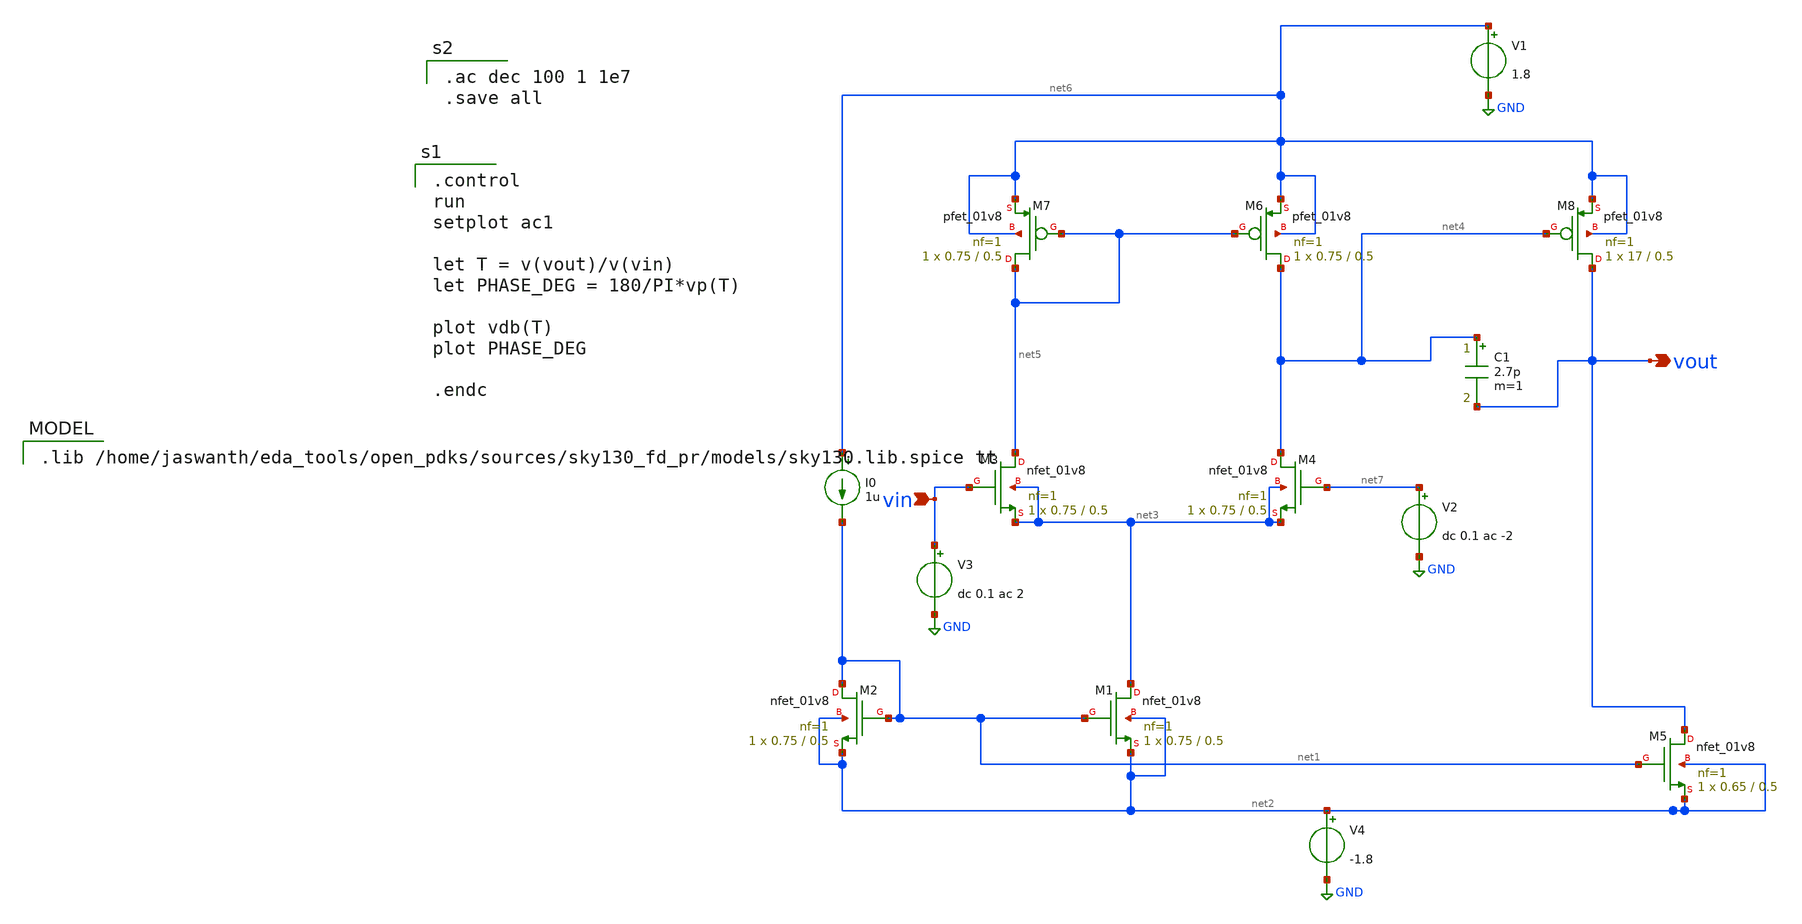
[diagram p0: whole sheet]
** sch_path: TwoStage_OpAmp/TwoStage_Main.sch
**.subckt TwoStage_Main vout vin
*.opin vout
*.ipin vin
XM1 net3 net1 net2 net2 sky130_fd_pr__nfet_01v8 L=0.5 W=0.75 nf=1 ad='int((1 + 1)/2) * 0.75 / 1 * 0.29'
+ as='int((1 + 2)/2) * 0.75 / 1 * 0.29' pd='2*int((1 + 1)/2) * (0.75 / 1 + 0.29)' ps='2*int((1 + 2)/2) * (0.75 / 1 + 0.29)'
+ nrd='0.29 / 0.75 ' nrs='0.29 / 0.75 ' sa=0 sb=0 sd=0 mult=1 m=1
XM2 net1 net1 net2 net2 sky130_fd_pr__nfet_01v8 L=0.5 W=0.75 nf=1 ad='int((1 + 1)/2) * 0.75 / 1 * 0.29'
+ as='int((1 + 2)/2) * 0.75 / 1 * 0.29' pd='2*int((1 + 1)/2) * (0.75 / 1 + 0.29)' ps='2*int((1 + 2)/2) * (0.75 / 1 + 0.29)'
+ nrd='0.29 / 0.75 ' nrs='0.29 / 0.75 ' sa=0 sb=0 sd=0 mult=1 m=1
XM3 net5 vin net3 net3 sky130_fd_pr__nfet_01v8 L=0.5 W=0.75 nf=1 ad='int((1 + 1)/2) * 0.75 / 1 * 0.29'
+ as='int((1 + 2)/2) * 0.75 / 1 * 0.29' pd='2*int((1 + 1)/2) * (0.75 / 1 + 0.29)' ps='2*int((1 + 2)/2) * (0.75 / 1 + 0.29)'
+ nrd='0.29 / 0.75 ' nrs='0.29 / 0.75 ' sa=0 sb=0 sd=0 mult=1 m=1
XM4 net4 net7 net3 net3 sky130_fd_pr__nfet_01v8 L=0.5 W=0.75 nf=1 ad='int((1 + 1)/2) * 0.75 / 1 * 0.29'
+ as='int((1 + 2)/2) * 0.75 / 1 * 0.29' pd='2*int((1 + 1)/2) * (0.75 / 1 + 0.29)' ps='2*int((1 + 2)/2) * (0.75 / 1 + 0.29)'
+ nrd='0.29 / 0.75 ' nrs='0.29 / 0.75 ' sa=0 sb=0 sd=0 mult=1 m=1
XM5 vout net1 net2 net2 sky130_fd_pr__nfet_01v8 L=0.5 W=0.65 nf=1 ad='int((1 + 1)/2) * 0.65 / 1 * 0.29'
+ as='int((1 + 2)/2) * 0.65 / 1 * 0.29' pd='2*int((1 + 1)/2) * (0.65 / 1 + 0.29)' ps='2*int((1 + 2)/2) * (0.65 / 1 + 0.29)'
+ nrd='0.29 / 0.65 ' nrs='0.29 / 0.65 ' sa=0 sb=0 sd=0 mult=1 m=1
XM6 net4 net5 net6 net6 sky130_fd_pr__pfet_01v8 L=0.5 W=0.75 nf=1 ad='int((1 + 1)/2) * 0.75 / 1 * 0.29'
+ as='int((1 + 2)/2) * 0.75 / 1 * 0.29' pd='2*int((1 + 1)/2) * (0.75 / 1 + 0.29)' ps='2*int((1 + 2)/2) * (0.75 / 1 + 0.29)'
+ nrd='0.29 / 0.75 ' nrs='0.29 / 0.75 ' sa=0 sb=0 sd=0 mult=1 m=1
XM7 net5 net5 net6 net6 sky130_fd_pr__pfet_01v8 L=0.5 W=0.75 nf=1 ad='int((1 + 1)/2) * 0.75 / 1 * 0.29'
+ as='int((1 + 2)/2) * 0.75 / 1 * 0.29' pd='2*int((1 + 1)/2) * (0.75 / 1 + 0.29)' ps='2*int((1 + 2)/2) * (0.75 / 1 + 0.29)'
+ nrd='0.29 / 0.75 ' nrs='0.29 / 0.75 ' sa=0 sb=0 sd=0 mult=1 m=1
XM8 vout net4 net6 net6 sky130_fd_pr__pfet_01v8 L=0.5 W=17 nf=1 ad='int((1 + 1)/2) * 17 / 1 * 0.29' as='int((1 + 2)/2) * 17 / 1 * 0.29'
+ pd='2*int((1 + 1)/2) * (17 / 1 + 0.29)' ps='2*int((1 + 2)/2) * (17 / 1 + 0.29)' nrd='0.29 / 17 ' nrs='0.29 / 17 '
+ sa=0 sb=0 sd=0 mult=1 m=1
C1 net4 vout 2.7p m=1
V1 net6 GND 1.8
V2 net7 GND dc 0.1 ac -2
V3 vin GND dc 0.1 ac 2
I0 net6 net1 1u
V4 net2 GND -1.8
**** begin user architecture code

.control
run
setplot ac1

let T = v(vout)/v(vin)
let PHASE_DEG = 180/PI*vp(T)

plot vdb(T)
plot PHASE_DEG

.endc


.lib /home/jaswanth/eda_tools/open_pdks/sources/sky130_fd_pr/models/sky130.lib.spice tt


.ac dec 100 1 1e7
.save all

**** end user architecture code
**.ends
.GLOBAL GND
.end
